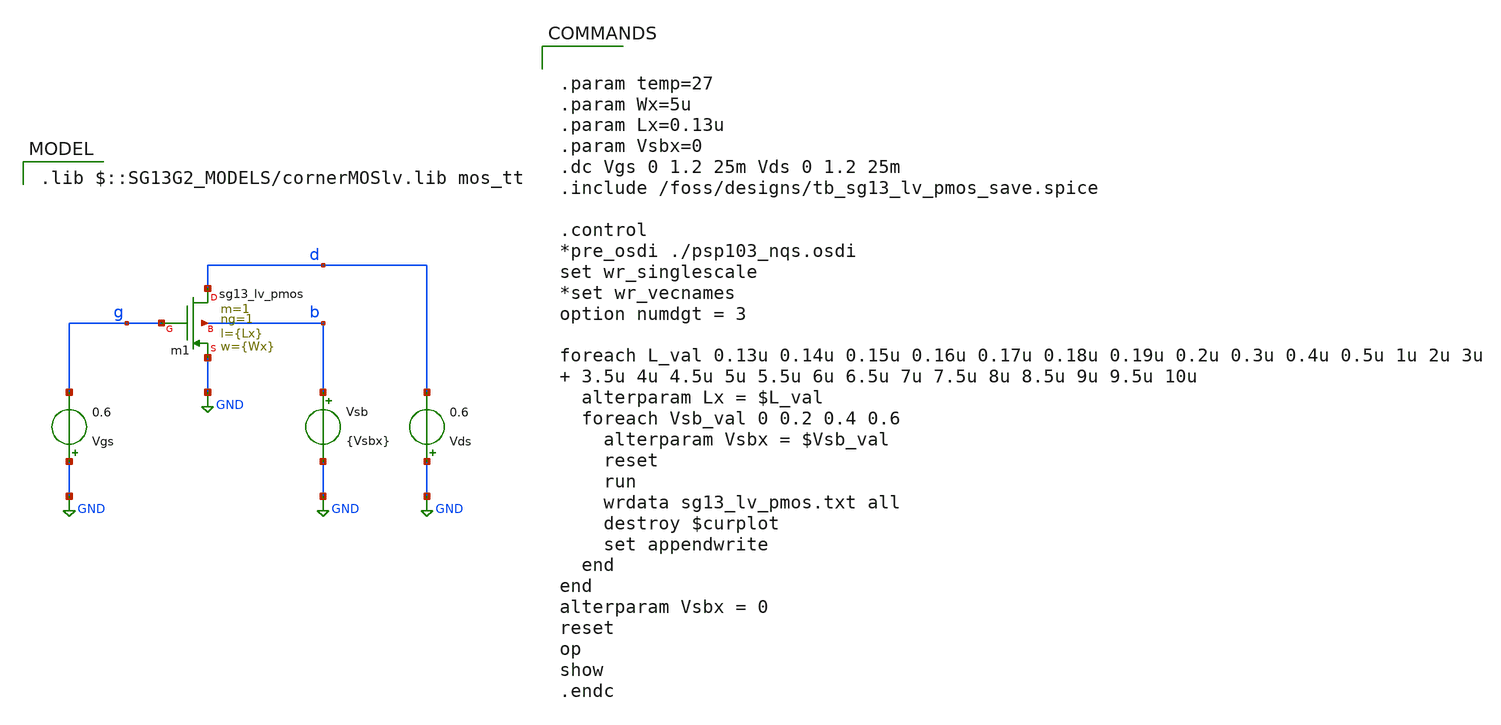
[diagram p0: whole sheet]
** sch_path: 4_Technology/src/tb_sg13_lv_pmos.sch
**.subckt tb_sg13_lv_pmos
Vgs GND g 0.6
Vds GND d 0.6
Vsb b GND {Vsbx}
Xm1 d g GND b sg13_lv_pmos w={Wx} l={Lx} ng=1 m=1 mm_ok=1
**** begin user architecture code
 .lib $::SG13G2_MODELS/cornerMOSlv.lib mos_tt



.param temp=27
.param Wx=5u
.param Lx=0.13u
.param Vsbx=0
.dc Vgs 0 1.2 25m Vds 0 1.2 25m
.include /foss/designs/tb_sg13_lv_pmos_save.spice

.control
*pre_osdi ./psp103_nqs.osdi
set wr_singlescale
*set wr_vecnames
option numdgt = 3

foreach L_val 0.13u 0.14u 0.15u 0.16u 0.17u 0.18u 0.19u 0.2u 0.3u 0.4u 0.5u 1u 2u 3u   3.5u 4u 4.5u
+ 5u 5.5u 6u 6.5u 7u 7.5u 8u 8.5u 9u 9.5u 10u
  alterparam Lx = $L_val
  foreach Vsb_val 0 0.2 0.4 0.6
    alterparam Vsbx = $Vsb_val
    reset
    run
    wrdata sg13_lv_pmos.txt all
    destroy $curplot
    set appendwrite
  end
end
alterparam Vsbx = 0
reset
op
show
.endc


**** end user architecture code
**.ends
.GLOBAL GND
.end
